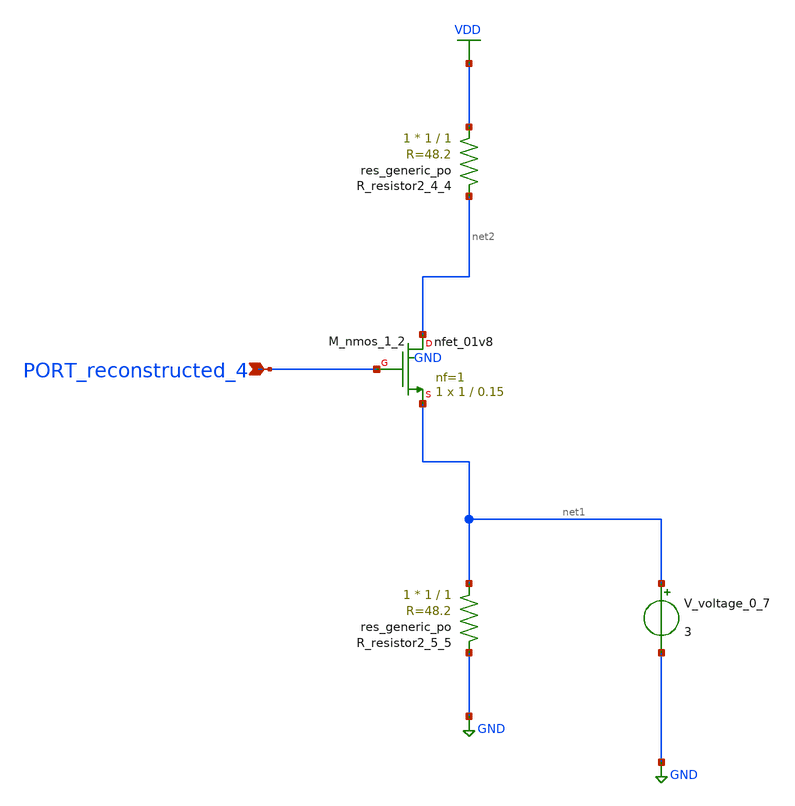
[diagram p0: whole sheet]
** sch_path: schematics/AMSNet/161.sch
**.subckt 161 PORT_reconstructed_4
*.ipin PORT_reconstructed_4
XM_nmos_1_2 net2 PORT_reconstructed_4 net1 GND sky130_fd_pr__nfet_01v8 L=0.15 W=1 nf=1 ad='int((1 + 1)/2) * 1 / 1 * 0.29'
+ as='int((1 + 2)/2) * 1 / 1 * 0.29' pd='2*int((1 + 1)/2) * (1 / 1 + 0.29)' ps='2*int((1 + 2)/2) * (1 / 1 + 0.29)'
+ nrd='0.29 / 1 ' nrs='0.29 / 1 ' sa=0 sb=0 sd=0 mult=1 m=1
XR_resistor2_4_4 VDD net2 sky130_fd_pr__res_generic_po W=1 L=1 m=1
XR_resistor2_5_5 net1 GND sky130_fd_pr__res_generic_po W=1 L=1 m=1
V_voltage_0_7 net1 GND 3
**.ends
.GLOBAL GND
.GLOBAL VDD
.end
